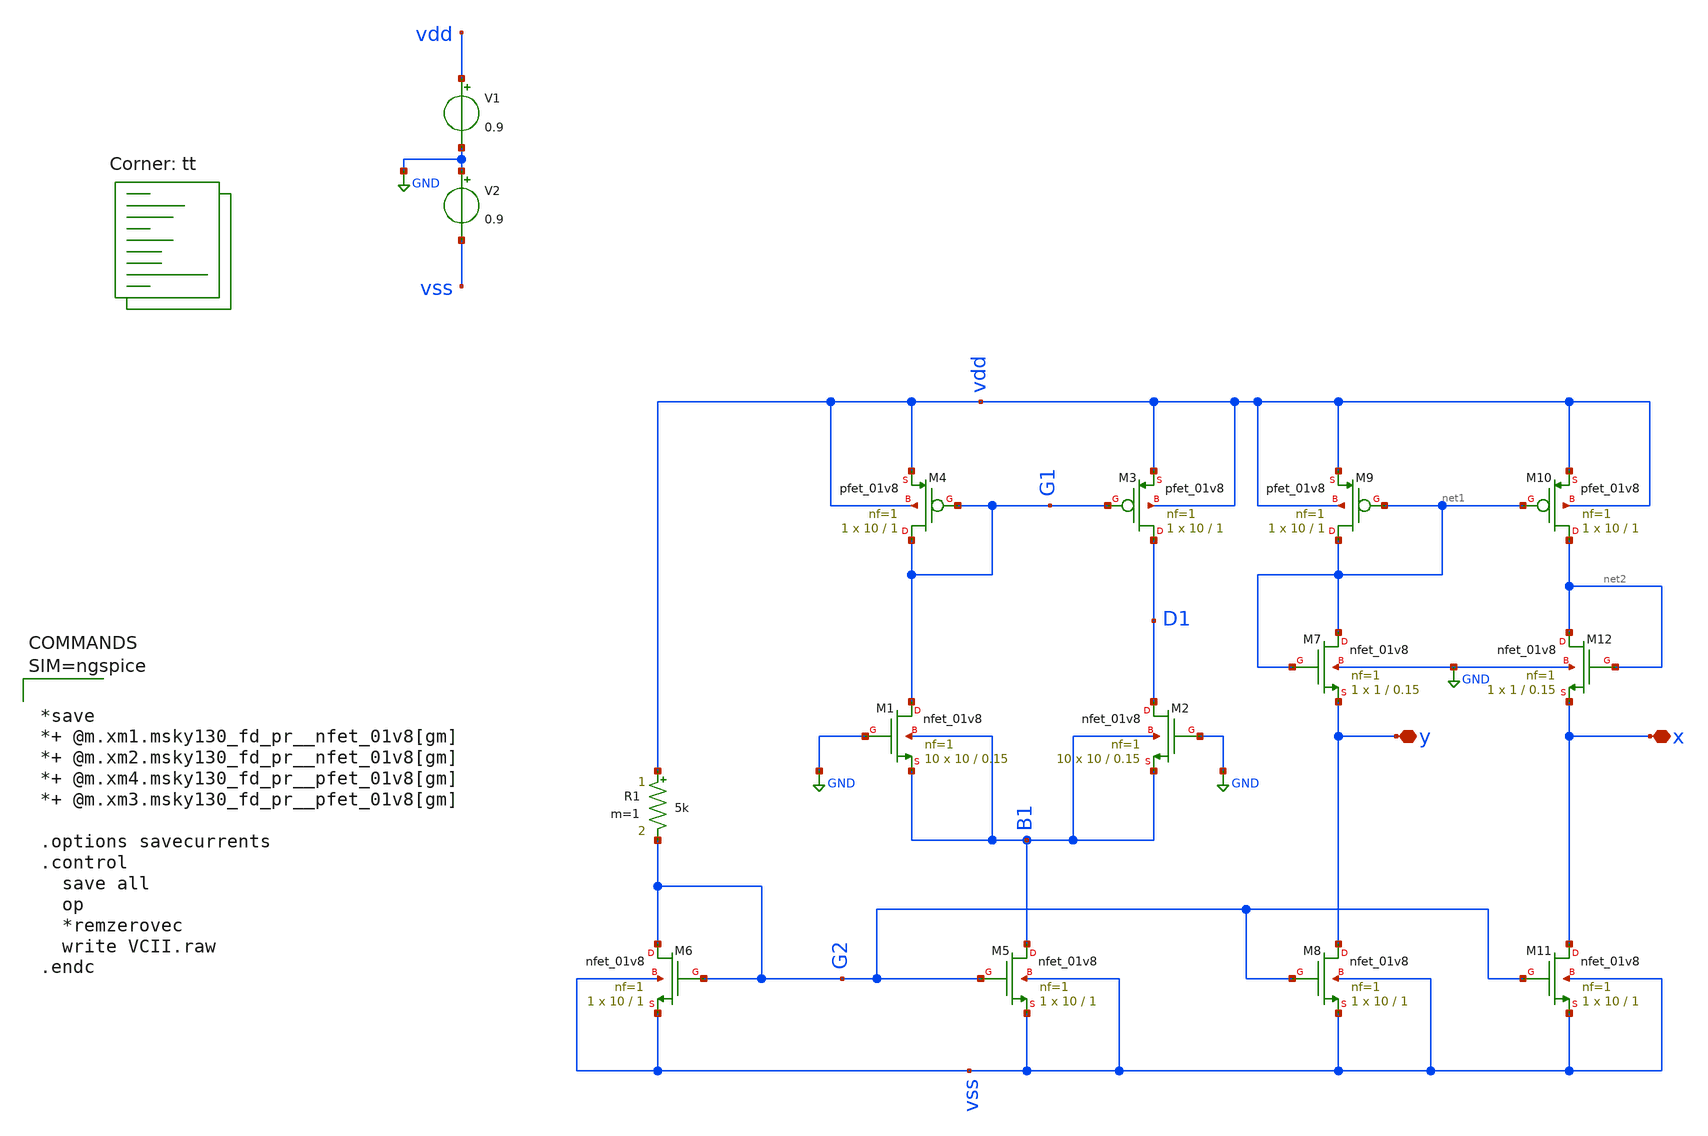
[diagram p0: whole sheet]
** sch_path: xschem/VCII.sch
**.subckt VCII x y
*.iopin x
*.iopin y
XM1 G1 GND B1 B1 sky130_fd_pr__nfet_01v8 L=0.15 W=10 nf=1 ad='int((nf+1)/2) * W/nf * 0.29' as='int((nf+2)/2) * W/nf * 0.29'
+ pd='2*int((nf+1)/2) * (W/nf + 0.29)' ps='2*int((nf+2)/2) * (W/nf + 0.29)' nrd='0.29 / W' nrs='0.29 / W'
+ sa=0 sb=0 sd=0 mult=10 m=10
XM2 D1 GND B1 B1 sky130_fd_pr__nfet_01v8 L=0.15 W=10 nf=1 ad='int((nf+1)/2) * W/nf * 0.29' as='int((nf+2)/2) * W/nf * 0.29'
+ pd='2*int((nf+1)/2) * (W/nf + 0.29)' ps='2*int((nf+2)/2) * (W/nf + 0.29)' nrd='0.29 / W' nrs='0.29 / W'
+ sa=0 sb=0 sd=0 mult=10 m=10
XM3 D1 G1 vdd vdd sky130_fd_pr__pfet_01v8 L=1 W=10 nf=1 ad='int((nf+1)/2) * W/nf * 0.29' as='int((nf+2)/2) * W/nf * 0.29'
+ pd='2*int((nf+1)/2) * (W/nf + 0.29)' ps='2*int((nf+2)/2) * (W/nf + 0.29)' nrd='0.29 / W' nrs='0.29 / W'
+ sa=0 sb=0 sd=0 mult=1 m=1
XM4 G1 G1 vdd vdd sky130_fd_pr__pfet_01v8 L=1 W=10 nf=1 ad='int((nf+1)/2) * W/nf * 0.29' as='int((nf+2)/2) * W/nf * 0.29'
+ pd='2*int((nf+1)/2) * (W/nf + 0.29)' ps='2*int((nf+2)/2) * (W/nf + 0.29)' nrd='0.29 / W' nrs='0.29 / W'
+ sa=0 sb=0 sd=0 mult=1 m=1
V1 vdd GND 0.9
V2 GND vss 0.9
XM5 B1 G2 vss vss sky130_fd_pr__nfet_01v8 L=1 W=10 nf=1 ad='int((nf+1)/2) * W/nf * 0.29' as='int((nf+2)/2) * W/nf * 0.29'
+ pd='2*int((nf+1)/2) * (W/nf + 0.29)' ps='2*int((nf+2)/2) * (W/nf + 0.29)' nrd='0.29 / W' nrs='0.29 / W'
+ sa=0 sb=0 sd=0 mult=1 m=1
XM6 G2 G2 vss vss sky130_fd_pr__nfet_01v8 L=1 W=10 nf=1 ad='int((nf+1)/2) * W/nf * 0.29' as='int((nf+2)/2) * W/nf * 0.29'
+ pd='2*int((nf+1)/2) * (W/nf + 0.29)' ps='2*int((nf+2)/2) * (W/nf + 0.29)' nrd='0.29 / W' nrs='0.29 / W'
+ sa=0 sb=0 sd=0 mult=1 m=1
R1 vdd G2 5k m=1
XM7 net1 net1 y GND sky130_fd_pr__nfet_01v8 L=0.15 W=1 nf=1 ad='int((nf+1)/2) * W/nf * 0.29' as='int((nf+2)/2) * W/nf * 0.29'
+ pd='2*int((nf+1)/2) * (W/nf + 0.29)' ps='2*int((nf+2)/2) * (W/nf + 0.29)' nrd='0.29 / W' nrs='0.29 / W'
+ sa=0 sb=0 sd=0 mult=1 m=1
XM8 y G2 vss vss sky130_fd_pr__nfet_01v8 L=1 W=10 nf=1 ad='int((nf+1)/2) * W/nf * 0.29' as='int((nf+2)/2) * W/nf * 0.29'
+ pd='2*int((nf+1)/2) * (W/nf + 0.29)' ps='2*int((nf+2)/2) * (W/nf + 0.29)' nrd='0.29 / W' nrs='0.29 / W'
+ sa=0 sb=0 sd=0 mult=1 m=1
XM9 net1 net1 vdd vdd sky130_fd_pr__pfet_01v8 L=1 W=10 nf=1 ad='int((nf+1)/2) * W/nf * 0.29' as='int((nf+2)/2) * W/nf * 0.29'
+ pd='2*int((nf+1)/2) * (W/nf + 0.29)' ps='2*int((nf+2)/2) * (W/nf + 0.29)' nrd='0.29 / W' nrs='0.29 / W'
+ sa=0 sb=0 sd=0 mult=1 m=1
XM10 net2 net1 vdd vdd sky130_fd_pr__pfet_01v8 L=1 W=10 nf=1 ad='int((nf+1)/2) * W/nf * 0.29' as='int((nf+2)/2) * W/nf * 0.29'
+ pd='2*int((nf+1)/2) * (W/nf + 0.29)' ps='2*int((nf+2)/2) * (W/nf + 0.29)' nrd='0.29 / W' nrs='0.29 / W'
+ sa=0 sb=0 sd=0 mult=1 m=1
XM11 x G2 vss vss sky130_fd_pr__nfet_01v8 L=1 W=10 nf=1 ad='int((nf+1)/2) * W/nf * 0.29' as='int((nf+2)/2) * W/nf * 0.29'
+ pd='2*int((nf+1)/2) * (W/nf + 0.29)' ps='2*int((nf+2)/2) * (W/nf + 0.29)' nrd='0.29 / W' nrs='0.29 / W'
+ sa=0 sb=0 sd=0 mult=1 m=1
XM12 net2 net2 x GND sky130_fd_pr__nfet_01v8 L=0.15 W=1 nf=1 ad='int((nf+1)/2) * W/nf * 0.29' as='int((nf+2)/2) * W/nf * 0.29'
+ pd='2*int((nf+1)/2) * (W/nf + 0.29)' ps='2*int((nf+2)/2) * (W/nf + 0.29)' nrd='0.29 / W' nrs='0.29 / W'
+ sa=0 sb=0 sd=0 mult=1 m=1
**** begin user architecture code



*save
*+ @m.xm1.msky130_fd_pr__nfet_01v8[gm]
*+ @m.xm2.msky130_fd_pr__nfet_01v8[gm]
*+ @m.xm4.msky130_fd_pr__pfet_01v8[gm]
*+ @m.xm3.msky130_fd_pr__pfet_01v8[gm]

.options savecurrents
.control
  save all
  op
  *remzerovec
  write VCII.raw
.endc



.lib $::SKYWATER_MODELS/sky130.lib.spice tt
**** end user architecture code
**.ends
.GLOBAL GND
.end
